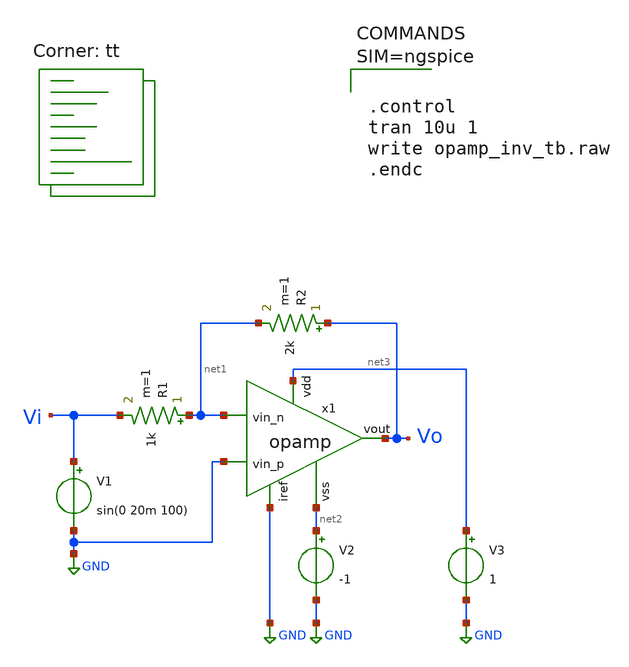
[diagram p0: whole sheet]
** sch_path: xschem/opamp_inv_tb.sch
**.subckt opamp_inv_tb
x1 net3 GND net1 GND Vo net2 opamp
R1 net1 Vi 1k m=1
R2 Vo net1 2k m=1
V1 Vi GND sin(0 20m 100)
V2 net2 GND -1
V3 net3 GND 1
**** begin user architecture code



.control
tran 10u 1
write opamp_inv_tb.raw
.endc



.lib $::SKYWATER_MODELS/sky130.lib.spice tt
**** end user architecture code
**.ends
.GLOBAL GND
.end
